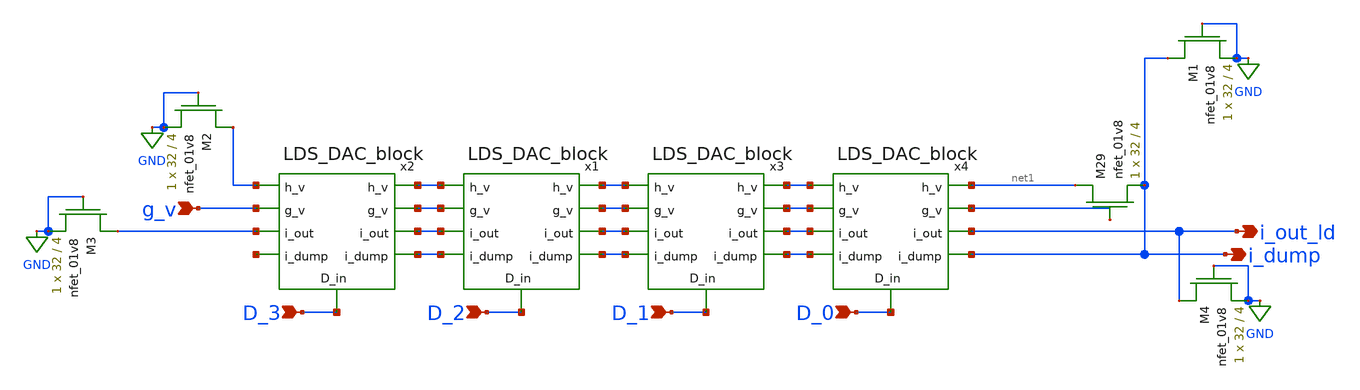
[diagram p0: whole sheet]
** sch_path: schemas/4bit_DAC_LDS.sch
**.subckt 4bit_DAC_LDS i_out_ld i_dump g_v D_3 D_2 D_1 D_0
*.opin i_out_ld
*.opin i_dump
*.ipin g_v
*.ipin D_3
*.ipin D_2
*.ipin D_1
*.ipin D_0
XM29 net1 g_v i_dump GND sky130_fd_pr__nfet_01v8 L=4 W=32 nf=1 ad='int((nf+1)/2) * W/nf * 0.29' as='int((nf+2)/2) * W/nf * 0.29'
+ pd='2*int((nf+1)/2) * (W/nf + 0.29)' ps='2*int((nf+2)/2) * (W/nf + 0.29)' nrd='0.29 / W' nrs='0.29 / W'
+ sa=0 sb=0 sd=0 mult=1 m=1
XM2 net1 GND GND GND sky130_fd_pr__nfet_01v8 L=4 W=32 nf=1 ad='int((nf+1)/2) * W/nf * 0.29' as='int((nf+2)/2) * W/nf * 0.29'
+ pd='2*int((nf+1)/2) * (W/nf + 0.29)' ps='2*int((nf+2)/2) * (W/nf + 0.29)' nrd='0.29 / W' nrs='0.29 / W'
+ sa=0 sb=0 sd=0 mult=1 m=1
XM3 i_out_ld GND GND GND sky130_fd_pr__nfet_01v8 L=4 W=32 nf=1 ad='int((nf+1)/2) * W/nf * 0.29' as='int((nf+2)/2) * W/nf * 0.29'
+ pd='2*int((nf+1)/2) * (W/nf + 0.29)' ps='2*int((nf+2)/2) * (W/nf + 0.29)' nrd='0.29 / W' nrs='0.29 / W'
+ sa=0 sb=0 sd=0 mult=1 m=1
XM1 i_dump GND GND GND sky130_fd_pr__nfet_01v8 L=4 W=32 nf=1 ad='int((nf+1)/2) * W/nf * 0.29' as='int((nf+2)/2) * W/nf * 0.29'
+ pd='2*int((nf+1)/2) * (W/nf + 0.29)' ps='2*int((nf+2)/2) * (W/nf + 0.29)' nrd='0.29 / W' nrs='0.29 / W'
+ sa=0 sb=0 sd=0 mult=1 m=1
XM4 i_out_ld GND GND GND sky130_fd_pr__nfet_01v8 L=4 W=32 nf=1 ad='int((nf+1)/2) * W/nf * 0.29' as='int((nf+2)/2) * W/nf * 0.29'
+ pd='2*int((nf+1)/2) * (W/nf + 0.29)' ps='2*int((nf+2)/2) * (W/nf + 0.29)' nrd='0.29 / W' nrs='0.29 / W'
+ sa=0 sb=0 sd=0 mult=1 m=1
x2 net1 g_v i_out_ld i_dump D_3 LDS_DAC_block
x1 net1 g_v i_out_ld i_dump D_2 LDS_DAC_block
x3 net1 g_v i_out_ld i_dump D_1 LDS_DAC_block
x4 net1 g_v i_out_ld i_dump D_0 LDS_DAC_block
**.ends

* expanding   symbol:  /home/mstopyra/Documents/DTILO/schemas/LDS_DAC_block.sym # of pins=9
** sym_path: schemas/LDS_DAC_block.sym
** sch_path: schemas/LDS_DAC_block.sch
.subckt LDS_DAC_block h_v g_v i_out i_dump D_in
*.opin i_dump
*.opin i_out
*.opin g_v
*.opin h_v
*.ipin g_v
*.ipin i_out
*.ipin i_dump
*.ipin h_v
*.ipin D_in
XM13 h_v g_v net1 GND sky130_fd_pr__nfet_01v8 L=4 W=32 nf=1 ad='int((nf+1)/2) * W/nf * 0.29' as='int((nf+2)/2) * W/nf * 0.29'
+ pd='2*int((nf+1)/2) * (W/nf + 0.29)' ps='2*int((nf+2)/2) * (W/nf + 0.29)' nrd='0.29 / W' nrs='0.29 / W'
+ sa=0 sb=0 sd=0 mult=1 m=1
XM14 i_out D_in h_v GND sky130_fd_pr__nfet_01v8 L=4 W=32 nf=1 ad='int((nf+1)/2) * W/nf * 0.29' as='int((nf+2)/2) * W/nf * 0.29'
+ pd='2*int((nf+1)/2) * (W/nf + 0.29)' ps='2*int((nf+2)/2) * (W/nf + 0.29)' nrd='0.29 / W' nrs='0.29 / W'
+ sa=0 sb=0 sd=0 mult=1 m=1
XM15 net1 g_v h_v GND sky130_fd_pr__nfet_01v8 L=4 W=32 nf=1 ad='int((nf+1)/2) * W/nf * 0.29' as='int((nf+2)/2) * W/nf * 0.29'
+ pd='2*int((nf+1)/2) * (W/nf + 0.29)' ps='2*int((nf+2)/2) * (W/nf + 0.29)' nrd='0.29 / W' nrs='0.29 / W'
+ sa=0 sb=0 sd=0 mult=1 m=1
XM16 h_v net2 i_dump GND sky130_fd_pr__nfet_01v8 L=4 W=32 nf=1 ad='int((nf+1)/2) * W/nf * 0.29' as='int((nf+2)/2) * W/nf * 0.29'
+ pd='2*int((nf+1)/2) * (W/nf + 0.29)' ps='2*int((nf+2)/2) * (W/nf + 0.29)' nrd='0.29 / W' nrs='0.29 / W'
+ sa=0 sb=0 sd=0 mult=1 m=1
XM19 net2 D_in GND GND sky130_fd_pr__nfet_01v8 L=4 W=32 nf=1 ad='int((nf+1)/2) * W/nf * 0.29' as='int((nf+2)/2) * W/nf * 0.29'
+ pd='2*int((nf+1)/2) * (W/nf + 0.29)' ps='2*int((nf+2)/2) * (W/nf + 0.29)' nrd='0.29 / W' nrs='0.29 / W'
+ sa=0 sb=0 sd=0 mult=1 m=1
XM20 net2 D_in VDD VDD sky130_fd_pr__pfet_01v8 L=4 W=32 nf=1 ad='int((nf+1)/2) * W/nf * 0.29' as='int((nf+2)/2) * W/nf * 0.29'
+ pd='2*int((nf+1)/2) * (W/nf + 0.29)' ps='2*int((nf+2)/2) * (W/nf + 0.29)' nrd='0.29 / W' nrs='0.29 / W'
+ sa=0 sb=0 sd=0 mult=1 m=1
.ends

.GLOBAL GND
.GLOBAL VDD
.end
